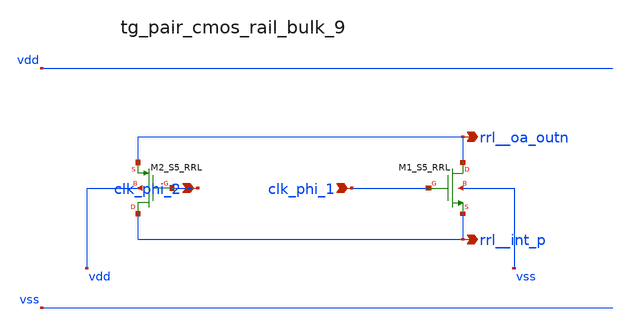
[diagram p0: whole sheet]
** sch_path: analog-db/raw/ia_004_fan_chopper_rrl/hier/blocks/tg_pair_cmos_rail_bulk_9.sch
**.subckt tg_pair_cmos_rail_bulk_9 clk_phi_2 clk_phi_1 rrl__oa_outn rrl__int_p
*.ipin clk_phi_2
*.ipin clk_phi_1
*.opin rrl__oa_outn
*.opin rrl__int_p
XM1_S5_RRL rrl__oa_outn clk_phi_1 rrl__int_p vss sg13_lv_nmos w=x_dut_xm1_s5_rrl_w
+ l=x_dut_xm1_s5_rrl_l ng=1 m=x_dut_xm1_s5_rrl_m
XM2_S5_RRL rrl__int_p clk_phi_2 rrl__oa_outn vdd sg13_lv_pmos w=x_dut_xm2_s5_rrl_w
+ l=x_dut_xm2_s5_rrl_l ng=1 m=x_dut_xm2_s5_rrl_m
**.ends
.end
